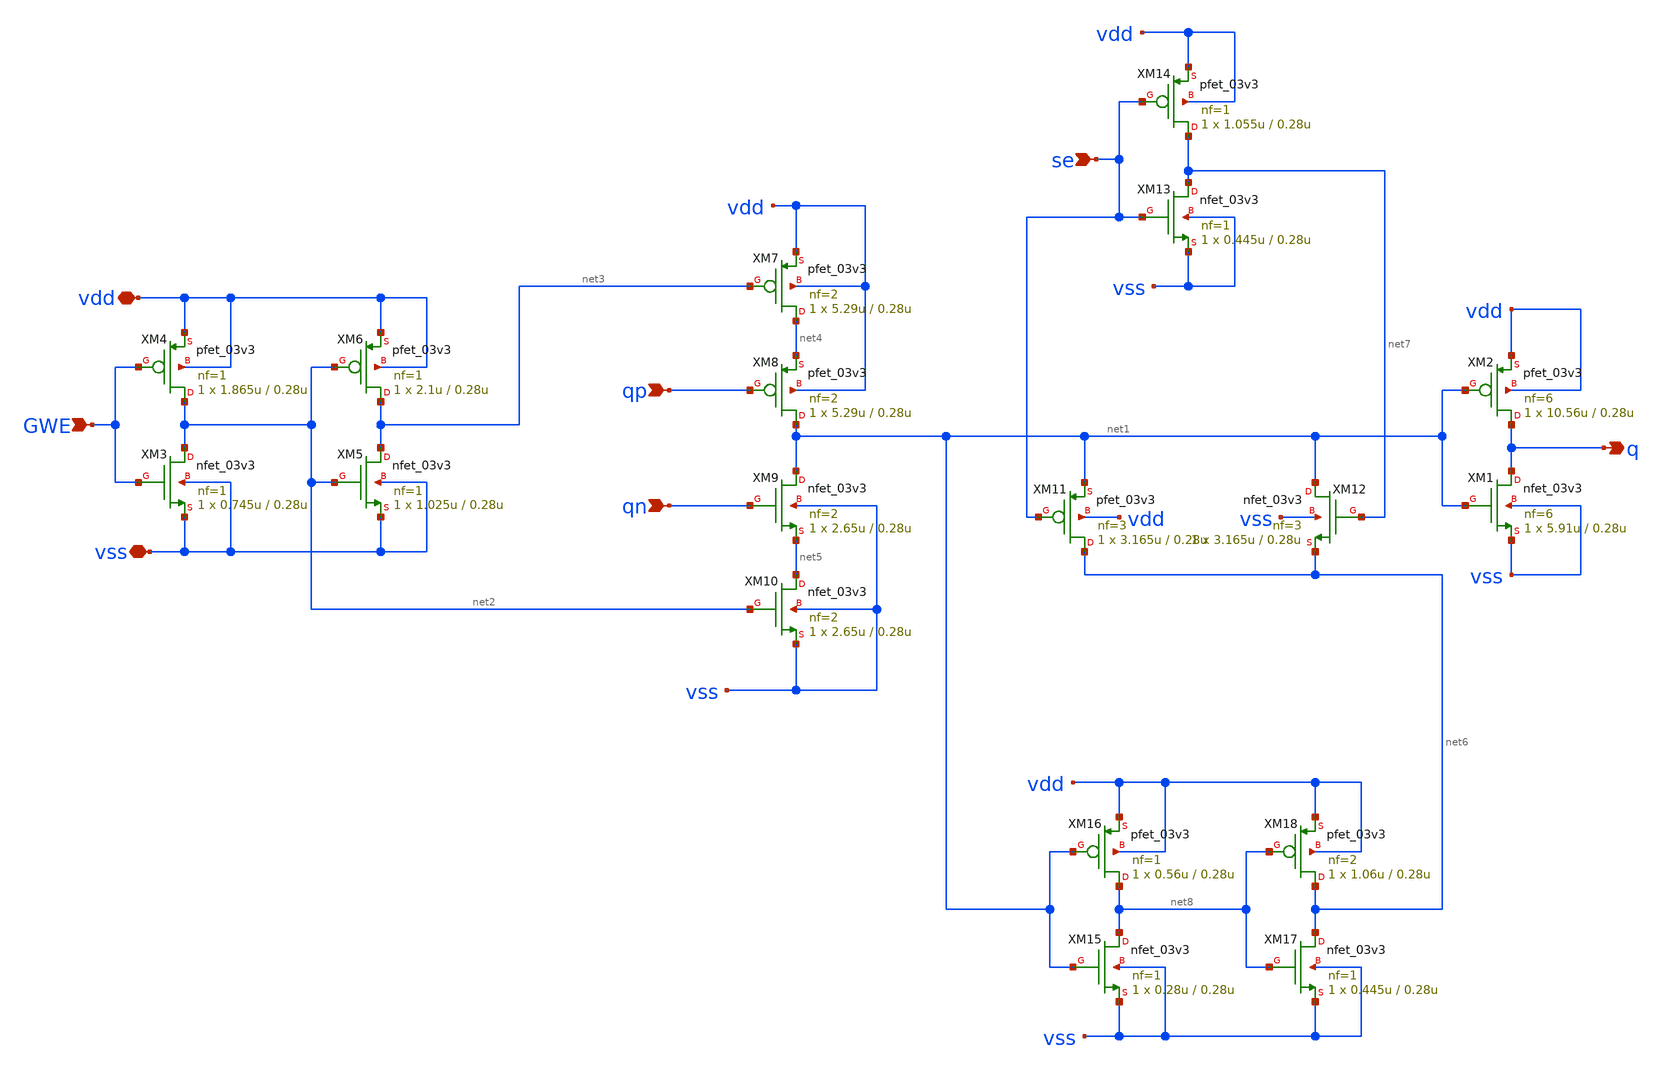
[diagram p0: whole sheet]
** sch_path: cells/gf180mcu_ocd_ip_sram__sram512x8m8wm1/xschem/outbuf_oe_3v512x8m81.sch
**.subckt outbuf_oe_3v512x8m81 q vdd vss GWE qp qn se
*.opin q
*.iopin vdd
*.iopin vss
*.ipin GWE
*.ipin qp
*.ipin qn
*.ipin se
XM1 q net1 vss vss nfet_03v3 L=0.28u W=5.91u nf=6 ad='int((nf+1)/2) * W/nf * 0.18u' as='int((nf+2)/2) * W/nf * 0.18u'
+ pd='2*int((nf+1)/2) * (W/nf + 0.18u)' ps='2*int((nf+2)/2) * (W/nf + 0.18u)' nrd='0.18u / W' nrs='0.18u / W'
+ sa=0 sb=0 sd=0 m=1
XM2 q net1 vdd vdd pfet_03v3 L=0.28u W=10.56u nf=6 ad='int((nf+1)/2) * W/nf * 0.18u' as='int((nf+2)/2) * W/nf * 0.18u'
+ pd='2*int((nf+1)/2) * (W/nf + 0.18u)' ps='2*int((nf+2)/2) * (W/nf + 0.18u)' nrd='0.18u / W' nrs='0.18u / W'
+ sa=0 sb=0 sd=0 m=1
XM3 net2 GWE vss vss nfet_03v3 L=0.28u W=0.745u nf=1 ad='int((nf+1)/2) * W/nf * 0.18u' as='int((nf+2)/2) * W/nf * 0.18u'
+ pd='2*int((nf+1)/2) * (W/nf + 0.18u)' ps='2*int((nf+2)/2) * (W/nf + 0.18u)' nrd='0.18u / W' nrs='0.18u / W'
+ sa=0 sb=0 sd=0 m=1
XM4 net2 GWE vdd vdd pfet_03v3 L=0.28u W=1.865u nf=1 ad='int((nf+1)/2) * W/nf * 0.18u' as='int((nf+2)/2) * W/nf * 0.18u'
+ pd='2*int((nf+1)/2) * (W/nf + 0.18u)' ps='2*int((nf+2)/2) * (W/nf + 0.18u)' nrd='0.18u / W' nrs='0.18u / W'
+ sa=0 sb=0 sd=0 m=1
XM5 net3 net2 vss vss nfet_03v3 L=0.28u W=1.025u nf=1 ad='int((nf+1)/2) * W/nf * 0.18u' as='int((nf+2)/2) * W/nf * 0.18u'
+ pd='2*int((nf+1)/2) * (W/nf + 0.18u)' ps='2*int((nf+2)/2) * (W/nf + 0.18u)' nrd='0.18u / W' nrs='0.18u / W'
+ sa=0 sb=0 sd=0 m=1
XM6 net3 net2 vdd vdd pfet_03v3 L=0.28u W=2.1u nf=1 ad='int((nf+1)/2) * W/nf * 0.18u' as='int((nf+2)/2) * W/nf * 0.18u'
+ pd='2*int((nf+1)/2) * (W/nf + 0.18u)' ps='2*int((nf+2)/2) * (W/nf + 0.18u)' nrd='0.18u / W' nrs='0.18u / W'
+ sa=0 sb=0 sd=0 m=1
XM7 net4 net3 vdd vdd pfet_03v3 L=0.28u W=5.29u nf=2 ad='int((nf+1)/2) * W/nf * 0.18u' as='int((nf+2)/2) * W/nf * 0.18u'
+ pd='2*int((nf+1)/2) * (W/nf + 0.18u)' ps='2*int((nf+2)/2) * (W/nf + 0.18u)' nrd='0.18u / W' nrs='0.18u / W'
+ sa=0 sb=0 sd=0 m=1
XM8 net1 qp net4 vdd pfet_03v3 L=0.28u W=5.29u nf=2 ad='int((nf+1)/2) * W/nf * 0.18u' as='int((nf+2)/2) * W/nf * 0.18u'
+ pd='2*int((nf+1)/2) * (W/nf + 0.18u)' ps='2*int((nf+2)/2) * (W/nf + 0.18u)' nrd='0.18u / W' nrs='0.18u / W'
+ sa=0 sb=0 sd=0 m=1
XM9 net1 qn net5 vss nfet_03v3 L=0.28u W=2.65u nf=2 ad='int((nf+1)/2) * W/nf * 0.18u' as='int((nf+2)/2) * W/nf * 0.18u'
+ pd='2*int((nf+1)/2) * (W/nf + 0.18u)' ps='2*int((nf+2)/2) * (W/nf + 0.18u)' nrd='0.18u / W' nrs='0.18u / W'
+ sa=0 sb=0 sd=0 m=1
XM10 net5 net2 vss vss nfet_03v3 L=0.28u W=2.65u nf=2 ad='int((nf+1)/2) * W/nf * 0.18u' as='int((nf+2)/2) * W/nf * 0.18u'
+ pd='2*int((nf+1)/2) * (W/nf + 0.18u)' ps='2*int((nf+2)/2) * (W/nf + 0.18u)' nrd='0.18u / W' nrs='0.18u / W'
+ sa=0 sb=0 sd=0 m=1
XM11 net6 se net1 vdd pfet_03v3 L=0.28u W=3.165u nf=3 ad='int((nf+1)/2) * W/nf * 0.18u' as='int((nf+2)/2) * W/nf * 0.18u'
+ pd='2*int((nf+1)/2) * (W/nf + 0.18u)' ps='2*int((nf+2)/2) * (W/nf + 0.18u)' nrd='0.18u / W' nrs='0.18u / W'
+ sa=0 sb=0 sd=0 m=1
XM12 net1 net7 net6 vss nfet_03v3 L=0.28u W=3.165u nf=3 ad='int((nf+1)/2) * W/nf * 0.18u' as='int((nf+2)/2) * W/nf * 0.18u'
+ pd='2*int((nf+1)/2) * (W/nf + 0.18u)' ps='2*int((nf+2)/2) * (W/nf + 0.18u)' nrd='0.18u / W' nrs='0.18u / W'
+ sa=0 sb=0 sd=0 m=1
XM13 net7 se vss vss nfet_03v3 L=0.28u W=0.445u nf=1 ad='int((nf+1)/2) * W/nf * 0.18u' as='int((nf+2)/2) * W/nf * 0.18u'
+ pd='2*int((nf+1)/2) * (W/nf + 0.18u)' ps='2*int((nf+2)/2) * (W/nf + 0.18u)' nrd='0.18u / W' nrs='0.18u / W'
+ sa=0 sb=0 sd=0 m=1
XM14 net7 se vdd vdd pfet_03v3 L=0.28u W=1.055u nf=1 ad='int((nf+1)/2) * W/nf * 0.18u' as='int((nf+2)/2) * W/nf * 0.18u'
+ pd='2*int((nf+1)/2) * (W/nf + 0.18u)' ps='2*int((nf+2)/2) * (W/nf + 0.18u)' nrd='0.18u / W' nrs='0.18u / W'
+ sa=0 sb=0 sd=0 m=1
XM15 net8 net1 vss vss nfet_03v3 L=0.28u W=0.28u nf=1 ad='int((nf+1)/2) * W/nf * 0.18u' as='int((nf+2)/2) * W/nf * 0.18u'
+ pd='2*int((nf+1)/2) * (W/nf + 0.18u)' ps='2*int((nf+2)/2) * (W/nf + 0.18u)' nrd='0.18u / W' nrs='0.18u / W'
+ sa=0 sb=0 sd=0 m=1
XM16 net8 net1 vdd vdd pfet_03v3 L=0.28u W=0.56u nf=1 ad='int((nf+1)/2) * W/nf * 0.18u' as='int((nf+2)/2) * W/nf * 0.18u'
+ pd='2*int((nf+1)/2) * (W/nf + 0.18u)' ps='2*int((nf+2)/2) * (W/nf + 0.18u)' nrd='0.18u / W' nrs='0.18u / W'
+ sa=0 sb=0 sd=0 m=1
XM17 net6 net8 vss vss nfet_03v3 L=0.28u W=0.445u nf=1 ad='int((nf+1)/2) * W/nf * 0.18u' as='int((nf+2)/2) * W/nf * 0.18u'
+ pd='2*int((nf+1)/2) * (W/nf + 0.18u)' ps='2*int((nf+2)/2) * (W/nf + 0.18u)' nrd='0.18u / W' nrs='0.18u / W'
+ sa=0 sb=0 sd=0 m=1
XM18 net6 net8 vdd vdd pfet_03v3 L=0.28u W=1.06u nf=2 ad='int((nf+1)/2) * W/nf * 0.18u' as='int((nf+2)/2) * W/nf * 0.18u'
+ pd='2*int((nf+1)/2) * (W/nf + 0.18u)' ps='2*int((nf+2)/2) * (W/nf + 0.18u)' nrd='0.18u / W' nrs='0.18u / W'
+ sa=0 sb=0 sd=0 m=1
**.ends
.end
